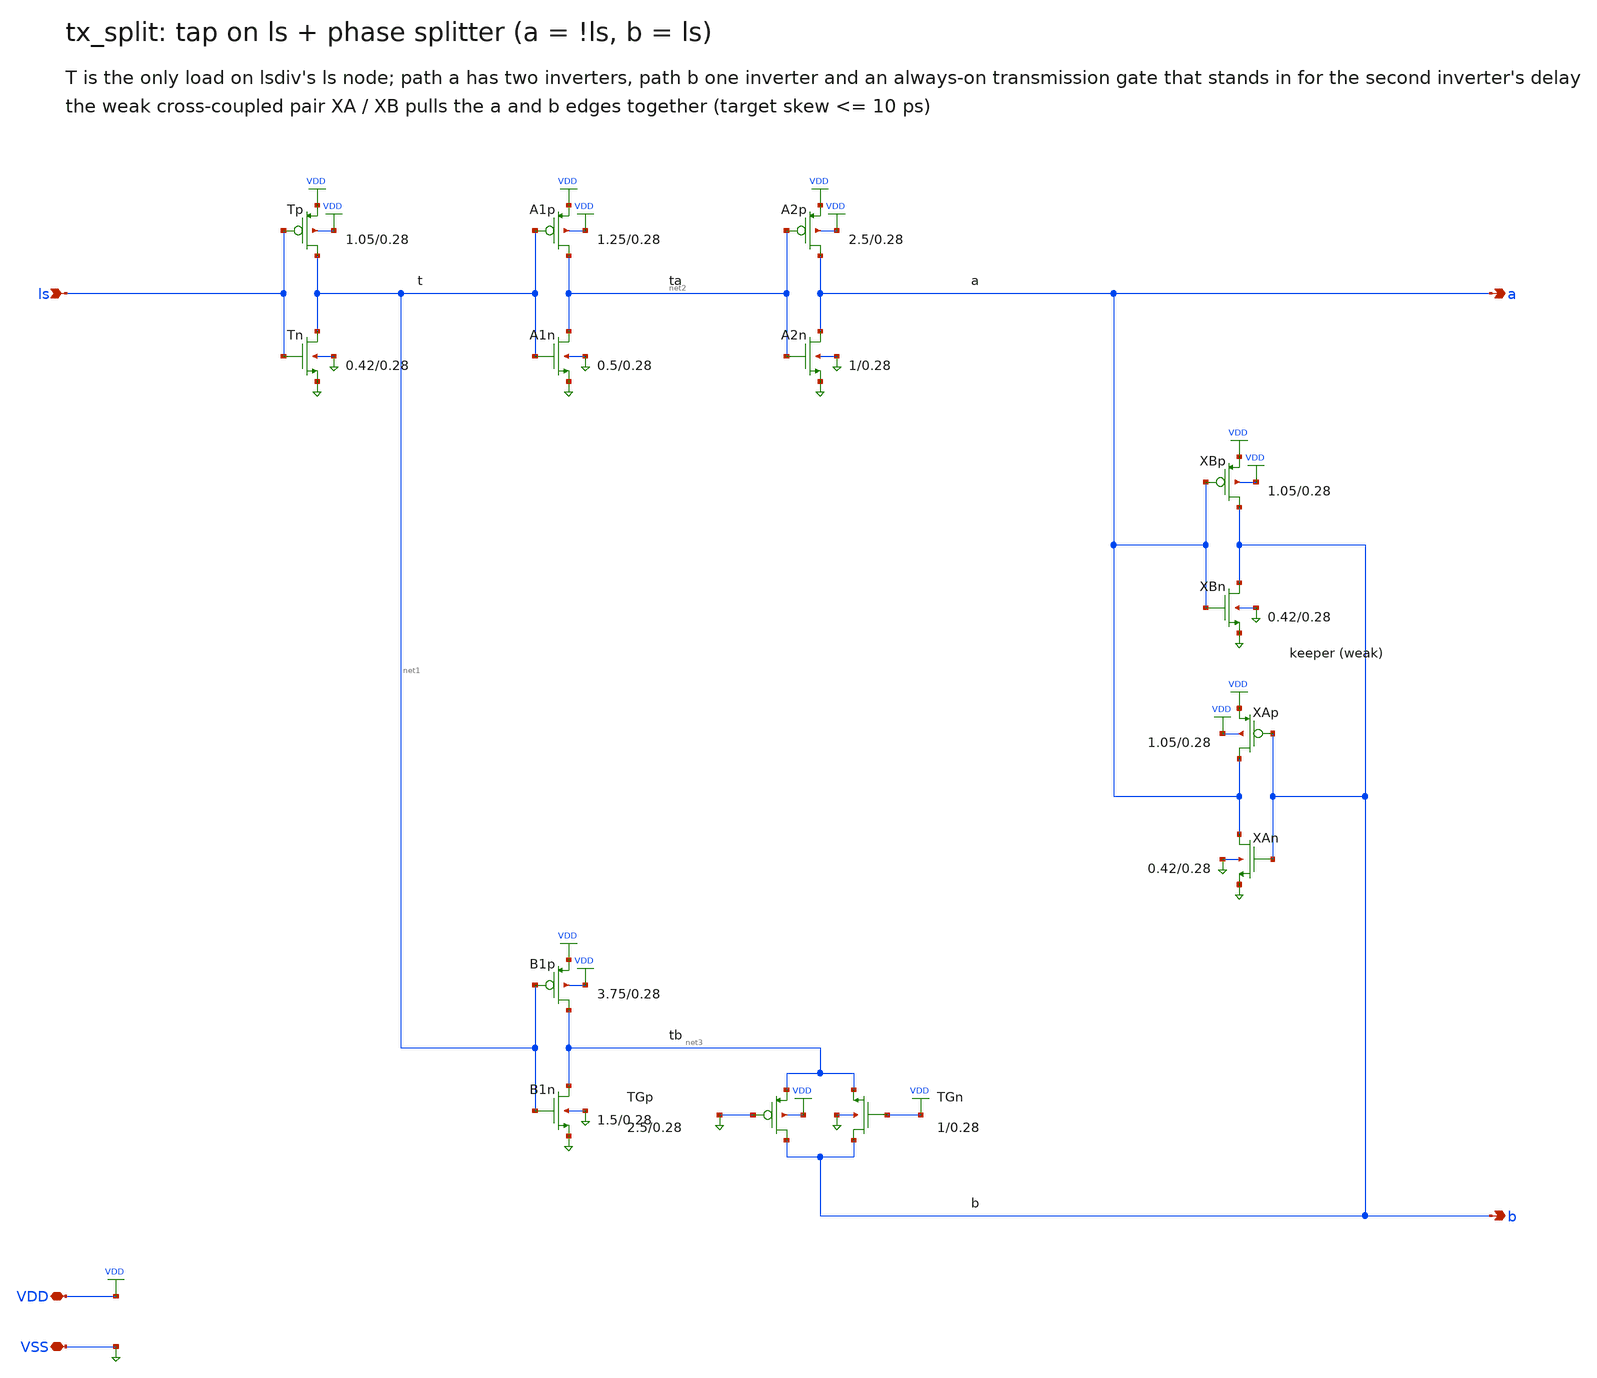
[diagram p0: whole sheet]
** sch_path: xschem/tx_split.sch
**.subckt tx_split VDD VSS ls a b
*.iopin VDD
*.iopin VSS
*.ipin ls
*.opin a
*.opin b
XTp net1 ls VDD VDD pfet_03v3 L=0.28u W=1.0499999999999998u nf=1 ad=0.5249999999999999p
+ as=0.5249999999999999p pd=3.0999999999999996u ps=3.0999999999999996u nrd=0 nrs=0 sa=0 sb=0 sd=0 m=1
XTn net1 ls VSS VSS nfet_03v3 L=0.28u W=0.41999999999999993u nf=1 ad=0.20999999999999996p
+ as=0.20999999999999996p pd=1.8399999999999999u ps=1.8399999999999999u nrd=0 nrs=0 sa=0 sb=0 sd=0 m=1
XA1p net2 net1 VDD VDD pfet_03v3 L=0.28u W=1.25u nf=1 ad=0.625p as=0.625p pd=3.5u ps=3.5u nrd=0
+ nrs=0 sa=0 sb=0 sd=0 m=1
XA1n net2 net1 VSS VSS nfet_03v3 L=0.28u W=0.5u nf=1 ad=0.25p as=0.25p pd=2.0u ps=2.0u nrd=0 nrs=0
+ sa=0 sb=0 sd=0 m=1
XA2p a net2 VDD VDD pfet_03v3 L=0.28u W=2.5u nf=1 ad=1.25p as=1.25p pd=6.0u ps=6.0u nrd=0 nrs=0 sa=0
+ sb=0 sd=0 m=1
XA2n a net2 VSS VSS nfet_03v3 L=0.28u W=1.0u nf=1 ad=0.5p as=0.5p pd=3.0u ps=3.0u nrd=0 nrs=0 sa=0
+ sb=0 sd=0 m=1
XB1p net3 net1 VDD VDD pfet_03v3 L=0.28u W=3.7499999999999996u nf=1 ad=1.8749999999999998p
+ as=1.8749999999999998p pd=8.5u ps=8.5u nrd=0 nrs=0 sa=0 sb=0 sd=0 m=1
XB1n net3 net1 VSS VSS nfet_03v3 L=0.28u W=1.5u nf=1 ad=0.75p as=0.75p pd=4.0u ps=4.0u nrd=0 nrs=0
+ sa=0 sb=0 sd=0 m=1
XTGp b VSS net3 VDD pfet_03v3 L=0.28u W=2.5u nf=1 ad=1.25p as=1.25p pd=6.0u ps=6.0u nrd=0 nrs=0 sa=0
+ sb=0 sd=0 m=1
XTGn b VDD net3 VSS nfet_03v3 L=0.28u W=1.0u nf=1 ad=0.5p as=0.5p pd=3.0u ps=3.0u nrd=0 nrs=0 sa=0
+ sb=0 sd=0 m=1
XXBp b a VDD VDD pfet_03v3 L=0.28u W=1.0499999999999998u nf=1 ad=0.5249999999999999p
+ as=0.5249999999999999p pd=3.0999999999999996u ps=3.0999999999999996u nrd=0 nrs=0 sa=0 sb=0 sd=0 m=1
XXBn b a VSS VSS nfet_03v3 L=0.28u W=0.41999999999999993u nf=1 ad=0.20999999999999996p
+ as=0.20999999999999996p pd=1.8399999999999999u ps=1.8399999999999999u nrd=0 nrs=0 sa=0 sb=0 sd=0 m=1
XXAp a b VDD VDD pfet_03v3 L=0.28u W=1.0499999999999998u nf=1 ad=0.5249999999999999p
+ as=0.5249999999999999p pd=3.0999999999999996u ps=3.0999999999999996u nrd=0 nrs=0 sa=0 sb=0 sd=0 m=1
XXAn a b VSS VSS nfet_03v3 L=0.28u W=0.41999999999999993u nf=1 ad=0.20999999999999996p
+ as=0.20999999999999996p pd=1.8399999999999999u ps=1.8399999999999999u nrd=0 nrs=0 sa=0 sb=0 sd=0 m=1
**.ends
.end
